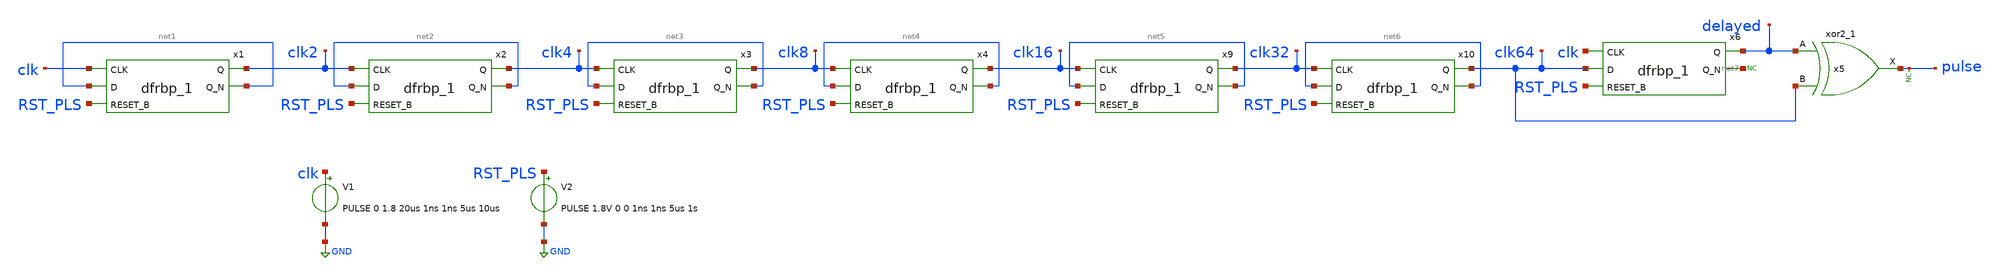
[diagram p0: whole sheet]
** sch_path: pulse_generator.sch
**.subckt pulse_generator
x1 clk net1 RST_PLS GND GND VCC VCC clk2 net1 sky130_fd_sc_hd__dfrbp_1
x2 clk2 net2 RST_PLS GND GND VCC VCC clk4 net2 sky130_fd_sc_hd__dfrbp_1
x3 clk4 net3 RST_PLS GND GND VCC VCC clk8 net3 sky130_fd_sc_hd__dfrbp_1
x4 clk8 net4 RST_PLS GND GND VCC VCC clk16 net4 sky130_fd_sc_hd__dfrbp_1
x5 delayed clk64 GND GND VCC VCC pulse sky130_fd_sc_hd__xor2_1
V1 clk GND PULSE 0 1.8 20us 1ns 1ns 5us 10us
V2 RST_PLS GND PULSE 1.8V 0 0 1ns 1ns 5us 1s
* noconn pulse
x6 clk clk64 RST_PLS GND GND VCC VCC delayed net7 sky130_fd_sc_hd__dfrbp_1
* noconn #net7
x9 clk16 net5 RST_PLS GND GND VCC VCC clk32 net5 sky130_fd_sc_hd__dfrbp_1
x10 clk32 net6 RST_PLS GND GND VCC VCC clk64 net6 sky130_fd_sc_hd__dfrbp_1
**** begin user architecture code
 .lib $::SKYWATER_MODELS/sky130.lib.spice tt
.include $::SKYWATER_STDCELLS/sky130_fd_sc_hd.spice



.options acct list
.temp 25
vvcc VCC 0 dc 1.8
*vvss GND 0 0
.control
tran 0.1u 400u
* plot a b+2 clk+4 reset_b+6 x+8 y+10 q+12 qlatch+14
plot RST_PLS-2 clk clk2+2 clk4+4 clk8+6 clk16+8 clk32+10 clk64+12 delayed+14 pulse+16
write pulse_generator.raw
.endc


**** end user architecture code
**.ends
.GLOBAL GND
.end
